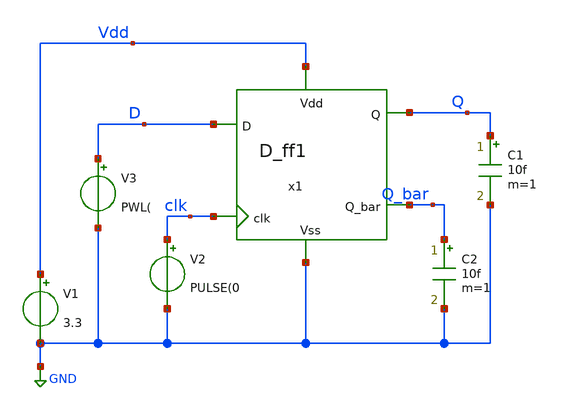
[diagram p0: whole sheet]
** sch_path: designs/TB_D_ff1.sch
**.subckt TB_D_ff1
x1 Vdd D Q Q_bar clk GND D_ff1
V1 Vdd GND 3.3
C1 Q GND 10f m=1
C2 Q_bar GND 10f m=1
V2 clk GND PULSE(0
V3 D GND PWL(
**** begin user architecture code

.include

**** end user architecture code
**.ends
.GLOBAL GND
.end
